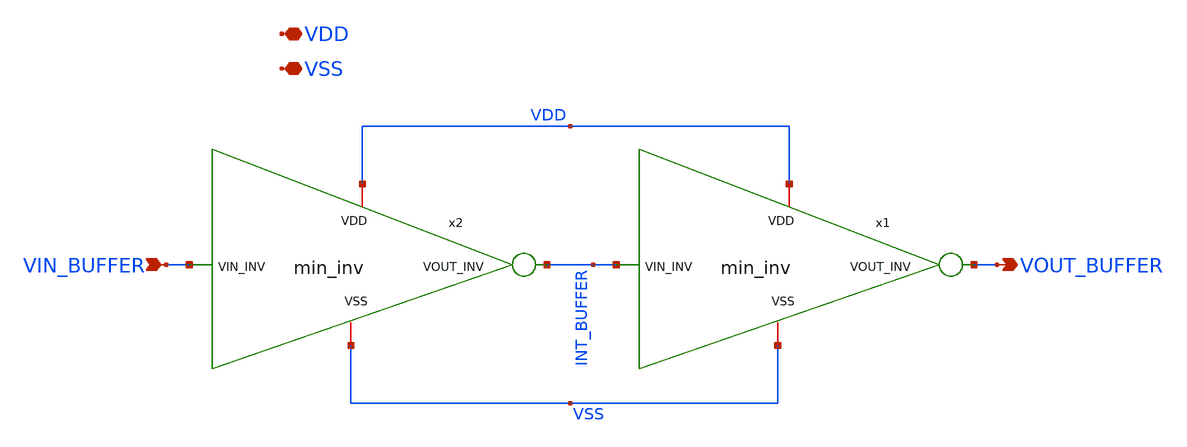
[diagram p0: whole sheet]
** sch_path: xschem/min_buffer.sch
**.subckt min_buffer VIN_BUFFER VOUT_BUFFER VDD VSS
*.ipin VIN_BUFFER
*.opin VOUT_BUFFER
*.iopin VDD
*.iopin VSS
x1 VDD VSS VOUT_BUFFER INT_BUFFER min_inv
x2 VDD VSS INT_BUFFER VIN_BUFFER min_inv
**.ends

* expanding   symbol:  min_inv.sym # of pins=4
** sym_path: xschem/min_inv.sym
** sch_path: xschem/min_inv.sch
.subckt min_inv VDD VSS VOUT_INV VIN_INV
*.iopin VDD
*.iopin VSS
*.ipin VIN_INV
*.opin VOUT_INV
XM2 VOUT_INV VIN_INV VSS VSS sky130_fd_pr__nfet_01v8 L=0.15 W=1 nf=1 ad='int((nf+1)/2) * W/nf * 0.29'
+ as='int((nf+2)/2) * W/nf * 0.29' pd='2*int((nf+1)/2) * (W/nf + 0.29)' ps='2*int((nf+2)/2) * (W/nf + 0.29)'
+ nrd='0.29 / W' nrs='0.29 / W' sa=0 sb=0 sd=0 mult=1 m=1
XM3 VOUT_INV VIN_INV VDD VDD sky130_fd_pr__pfet_01v8 L=0.15 W=1 nf=1 ad='int((nf+1)/2) * W/nf * 0.29'
+ as='int((nf+2)/2) * W/nf * 0.29' pd='2*int((nf+1)/2) * (W/nf + 0.29)' ps='2*int((nf+2)/2) * (W/nf + 0.29)'
+ nrd='0.29 / W' nrs='0.29 / W' sa=0 sb=0 sd=0 mult=1 m=1
.ends

.end
